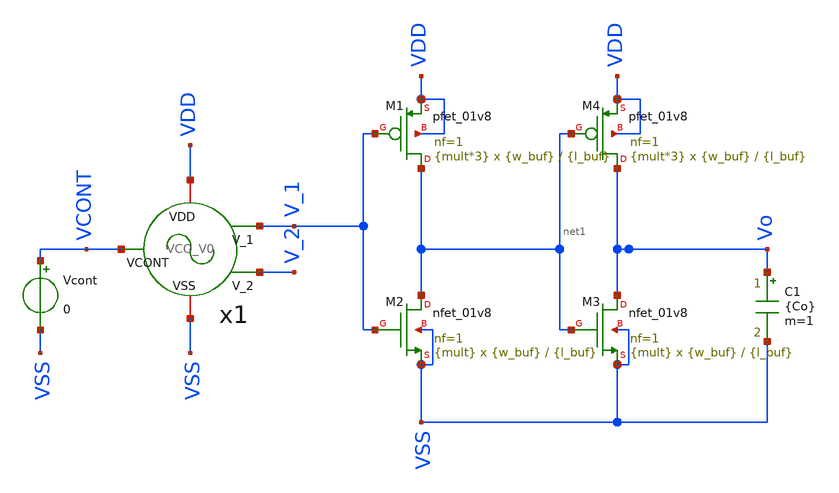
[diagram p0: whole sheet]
** sch_path: xschem/VCO/TB_Starved_VCO.sch
**.subckt TB_Starved_VCO
XM2 net1 V_1 VSS VSS sky130_fd_pr__nfet_01v8 L={l_buf} W={w_buf} nf=1 ad='int((nf+1)/2) * W/nf * 0.29'
+ as='int((nf+2)/2) * W/nf * 0.29' pd='2*int((nf+1)/2) * (W/nf + 0.29)' ps='2*int((nf+2)/2) * (W/nf + 0.29)'
+ nrd='0.29 / W' nrs='0.29 / W' sa=0 sb=0 sd=0 mult={mult} m={mult}
XM1 net1 V_1 VDD VDD sky130_fd_pr__pfet_01v8 L={l_buf} W={w_buf} nf=1 ad='int((nf+1)/2) * W/nf * 0.29'
+ as='int((nf+2)/2) * W/nf * 0.29' pd='2*int((nf+1)/2) * (W/nf + 0.29)' ps='2*int((nf+2)/2) * (W/nf + 0.29)'
+ nrd='0.29 / W' nrs='0.29 / W' sa=0 sb=0 sd=0 mult={mult*3} m={mult*3}
C1 Vo VSS {Co} m=1
XM3 Vo net1 VSS VSS sky130_fd_pr__nfet_01v8 L={l_buf} W={w_buf} nf=1 ad='int((nf+1)/2) * W/nf * 0.29'
+ as='int((nf+2)/2) * W/nf * 0.29' pd='2*int((nf+1)/2) * (W/nf + 0.29)' ps='2*int((nf+2)/2) * (W/nf + 0.29)'
+ nrd='0.29 / W' nrs='0.29 / W' sa=0 sb=0 sd=0 mult={mult} m={mult}
XM4 Vo net1 VDD VDD sky130_fd_pr__pfet_01v8 L={l_buf} W={w_buf} nf=1 ad='int((nf+1)/2) * W/nf * 0.29'
+ as='int((nf+2)/2) * W/nf * 0.29' pd='2*int((nf+1)/2) * (W/nf + 0.29)' ps='2*int((nf+2)/2) * (W/nf + 0.29)'
+ nrd='0.29 / W' nrs='0.29 / W' sa=0 sb=0 sd=0 mult={mult*3} m={mult*3}
Vcont VCONT VSS 0
x1 VCONT VSS VDD V_1 V_2 VCO_V0
**** begin user architecture code

.lib /opt/pdks/sky130A/libs.tech/ngspice/sky130.lib.spice tt
*.lib /opt/pdks/sky130A/libs.tech/ngspice/sky130.lib.spice ss
*.lib /opt/pdks/sky130A/libs.tech/ngspice/sky130.lib.spice ff
*.lib /opt/pdks/sky130A/libs.tech/ngspice/sky130.lib.spice sf
*.lib /opt/pdks/sky130A/libs.tech/ngspice/sky130.lib.spice fs


.param Co = 1p
.param mult = 1
.param w_buf = 1
.param l_buf = 0.15

.param vvcont = 0.5

vvdd vdd 0 dc 1.8
vvss vss 0 0
*vvcont VCONT 0 dc 0
*vvcont2 VCONT2 0 dc 0
*.option temp = 200
.ic v(V_1) = 0
.ic v(V_2) = 1.8
.save v(V_1) v(Vo)

.param SimTime =  10u
.csparam SimTime ={Simtime}
.csparam Tmargin = 1u





.param w_MP1 = 4
.param l_MP1 = 7
.param w_MP2 = 8
.param l_MP2 = 4
.param w_MP3 = 5
.param l_MP3 = 4
.param w_MP4 = 5
.param l_MP4 = 5

.param w_MN1 = 5
.param l_MN1 = 0.5
.param w_MN2 = 5
.param l_MN2 = 0.5
.param w_MN3 = 3
.param l_MN3 = 0.5
.param w_MN4 = 2
.param l_MN4 = 5





.save all
.tran 5n {SimTime}
*.tran 10n 1u
.csparam start = 10
.control
let Vtarg = 0.9
let f_sum = 0
let t_act = 0
let period_cont = 5
let period_cont2 = 6
run
meas tran T TRIG v(Vo) VAL = {Vtarg} RISE = {period_cont} TARG v(Vo) VAL = {Vtarg}  RISE = {period_cont2}
meas tran VCN AVG v(x1.x1.VCN) FROM=0 TO={SimTime}
let f =1/T
plot v(Vo)
plot v(x1.x1.VCN) v(x1.x1.VCP)
plot i(v.x1.x1.VIcont)
print f VCN
.endc


**** end user architecture code
**.ends
.end
